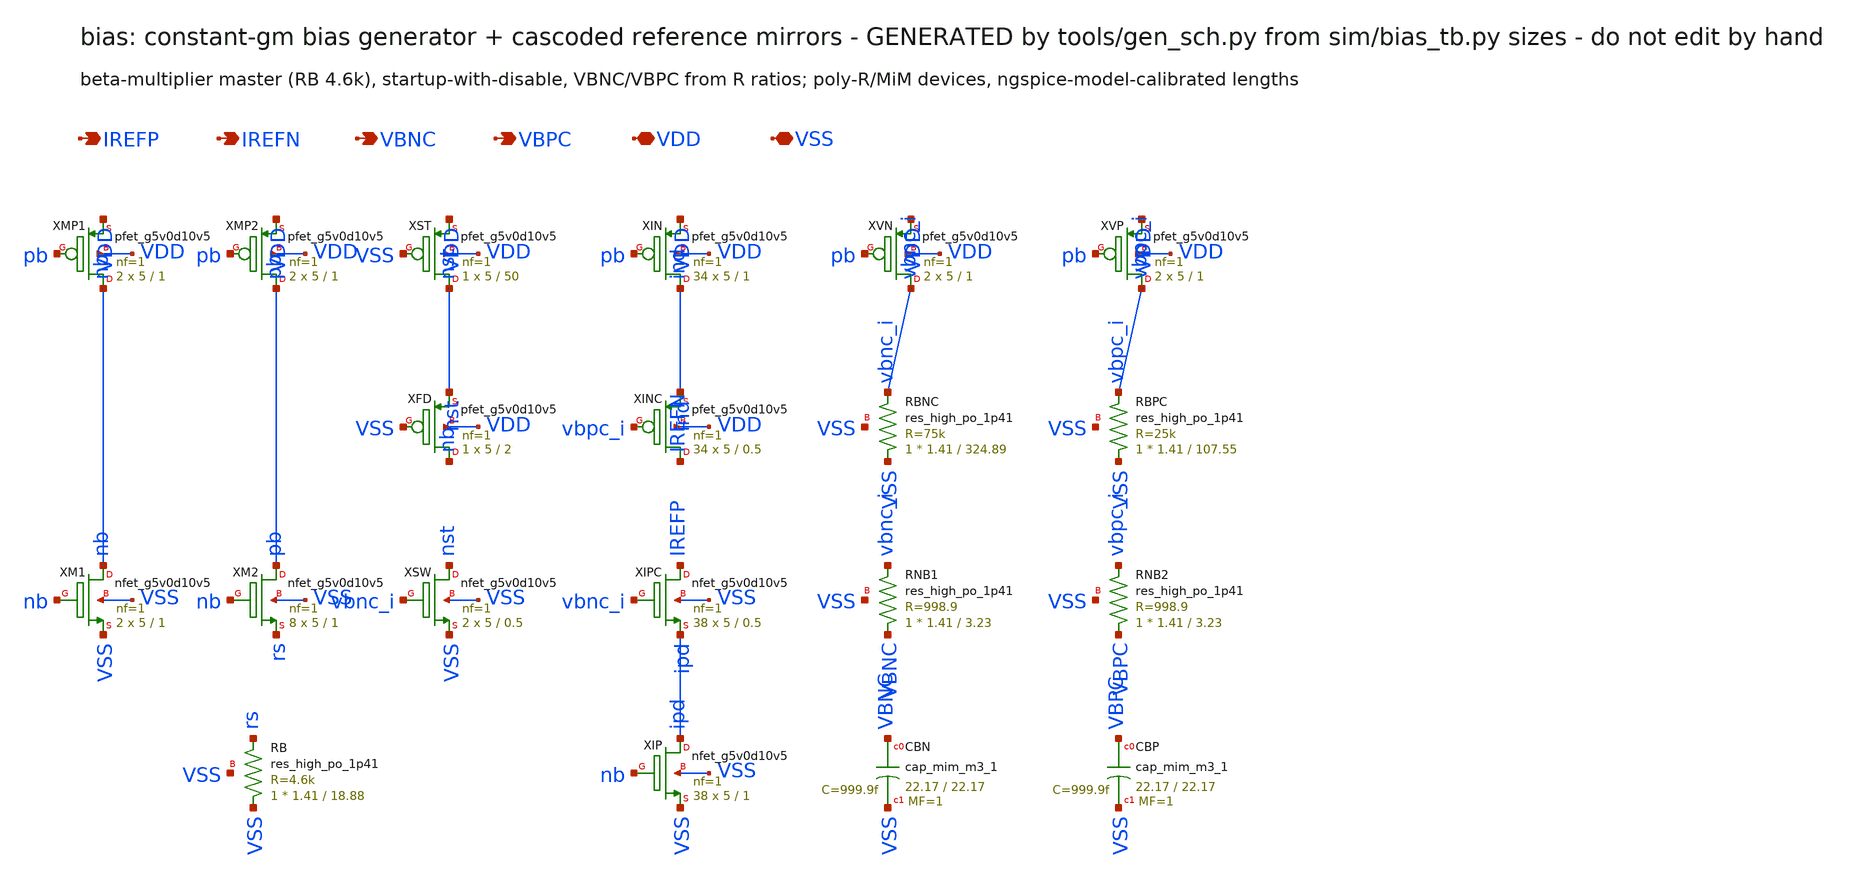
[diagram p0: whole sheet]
** sch_path: xschem/bias.sch
**.subckt bias IREFP IREFN VBNC VBPC VDD VSS
*.opin IREFP
*.opin IREFN
*.opin VBNC
*.opin VBPC
*.iopin VDD
*.iopin VSS
XXMP1 nb pb VDD VDD sky130_fd_pr__pfet_g5v0d10v5 L=1 W=5 nf=1 ad=0 as=0 pd=0 ps=0 nrd=0 nrs=0 sa=0
+ sb=0 sd=0 mult=2 m=2
XXMP2 pb pb VDD VDD sky130_fd_pr__pfet_g5v0d10v5 L=1 W=5 nf=1 ad=0 as=0 pd=0 ps=0 nrd=0 nrs=0 sa=0
+ sb=0 sd=0 mult=2 m=2
XXM1 nb nb VSS VSS sky130_fd_pr__nfet_g5v0d10v5 L=1 W=5 nf=1 ad=0 as=0 pd=0 ps=0 nrd=0 nrs=0 sa=0
+ sb=0 sd=0 mult=2 m=2
XXM2 pb nb rs VSS sky130_fd_pr__nfet_g5v0d10v5 L=1 W=5 nf=1 ad=0 as=0 pd=0 ps=0 nrd=0 nrs=0 sa=0
+ sb=0 sd=0 mult=8 m=8
XRB VSS rs VSS sky130_fd_pr__res_high_po_1p41 L=18.88 mult=1 m=1
XXST nst VSS VDD VDD sky130_fd_pr__pfet_g5v0d10v5 L=50 W=5 nf=1 ad=0 as=0 pd=0 ps=0 nrd=0 nrs=0 sa=0
+ sb=0 sd=0 mult=1 m=1
XXFD nb VSS nst VDD sky130_fd_pr__pfet_g5v0d10v5 L=2 W=5 nf=1 ad=0 as=0 pd=0 ps=0 nrd=0 nrs=0 sa=0
+ sb=0 sd=0 mult=1 m=1
XXSW nst vbnc_i VSS VSS sky130_fd_pr__nfet_g5v0d10v5 L=0.5 W=5 nf=1 ad=0 as=0 pd=0 ps=0 nrd=0 nrs=0
+ sa=0 sb=0 sd=0 mult=2 m=2
XXIN ind pb VDD VDD sky130_fd_pr__pfet_g5v0d10v5 L=1 W=5 nf=1 ad=0 as=0 pd=0 ps=0 nrd=0 nrs=0 sa=0
+ sb=0 sd=0 mult=34 m=34
XXINC IREFN vbpc_i ind VDD sky130_fd_pr__pfet_g5v0d10v5 L=0.5 W=5 nf=1 ad=0 as=0 pd=0 ps=0 nrd=0
+ nrs=0 sa=0 sb=0 sd=0 mult=34 m=34
XXIPC IREFP vbnc_i ipd VSS sky130_fd_pr__nfet_g5v0d10v5 L=0.5 W=5 nf=1 ad=0 as=0 pd=0 ps=0 nrd=0
+ nrs=0 sa=0 sb=0 sd=0 mult=38 m=38
XXIP ipd nb VSS VSS sky130_fd_pr__nfet_g5v0d10v5 L=1 W=5 nf=1 ad=0 as=0 pd=0 ps=0 nrd=0 nrs=0 sa=0
+ sb=0 sd=0 mult=38 m=38
XXVN vbnc_i pb VDD VDD sky130_fd_pr__pfet_g5v0d10v5 L=1 W=5 nf=1 ad=0 as=0 pd=0 ps=0 nrd=0 nrs=0
+ sa=0 sb=0 sd=0 mult=2 m=2
XRBNC VSS vbnc_i VSS sky130_fd_pr__res_high_po_1p41 L=324.89 mult=1 m=1
XRNB1 VBNC vbnc_i VSS sky130_fd_pr__res_high_po_1p41 L=3.23 mult=1 m=1
XCBN VBNC VSS sky130_fd_pr__cap_mim_m3_1 W=22.17 L=22.17 MF=1 m=1
XXVP vbpc_i pb VDD VDD sky130_fd_pr__pfet_g5v0d10v5 L=1 W=5 nf=1 ad=0 as=0 pd=0 ps=0 nrd=0 nrs=0
+ sa=0 sb=0 sd=0 mult=2 m=2
XRBPC VSS vbpc_i VSS sky130_fd_pr__res_high_po_1p41 L=107.55 mult=1 m=1
XRNB2 VBPC vbpc_i VSS sky130_fd_pr__res_high_po_1p41 L=3.23 mult=1 m=1
XCBP VBPC VSS sky130_fd_pr__cap_mim_m3_1 W=22.17 L=22.17 MF=1 m=1
**.ends
.end
